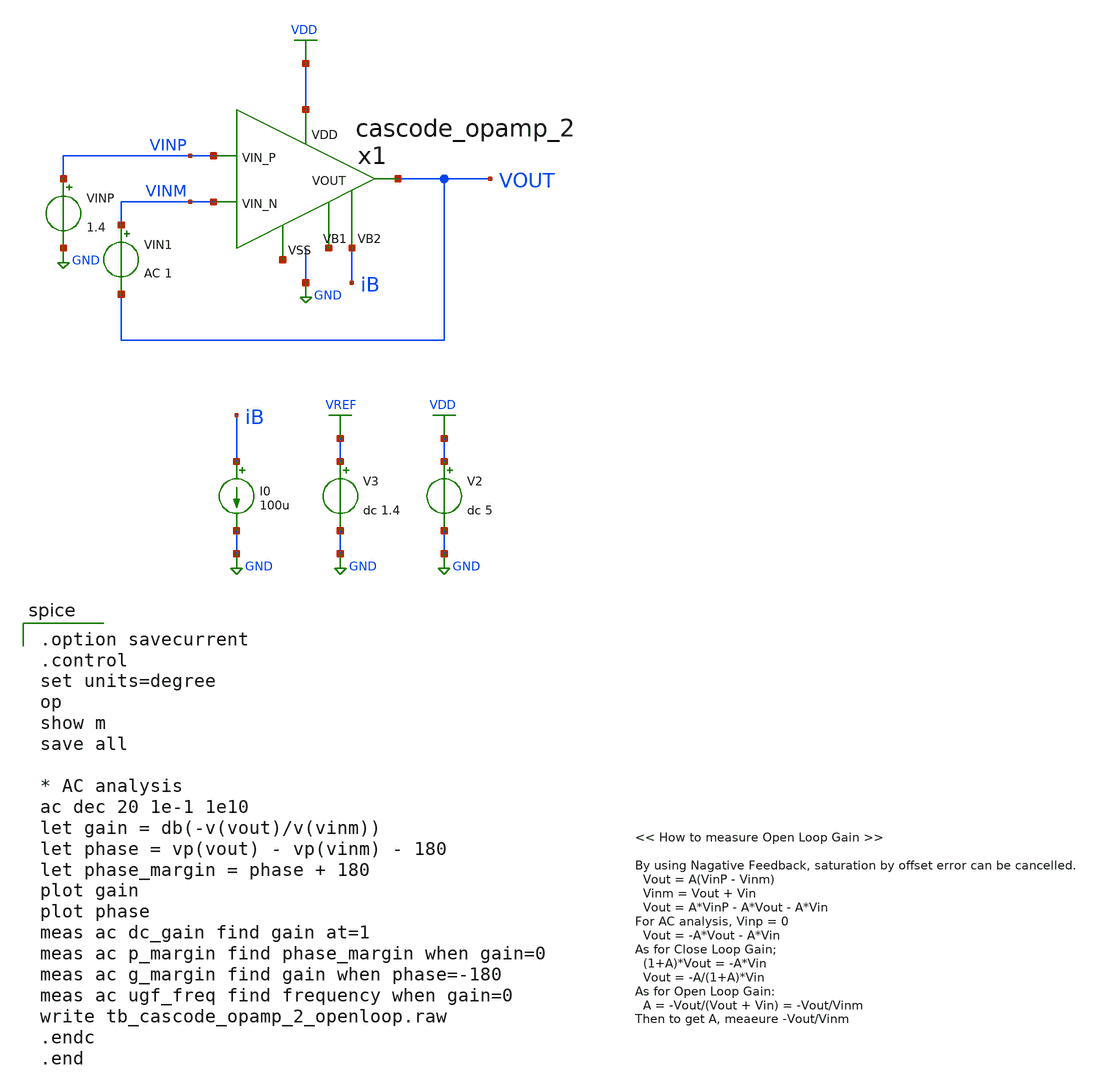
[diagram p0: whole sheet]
** sch_path: member_project/AM_Radio/Yamada3/xschem/tb_cascode_opamp_2_openloop.sch
**.subckt tb_cascode_opamp_2_openloop
V2 VDD GND dc 5
V3 VREF GND dc 1.4
I0 iB GND 100u
x1 VDD net1 VINP VINM VOUT iB net2 cascode_opamp_2
VIN1 VINM VOUT AC 1
VINP VINP GND 1.4
**** begin user architecture code
 .include $::LIB/ip62_models

.option savecurrent
.control
set units=degree
op
show m
save all

* AC analysis
ac dec 20 1e-1 1e10
let gain = db(-v(vout)/v(vinm))
let phase = vp(vout) - vp(vinm) - 180
let phase_margin = phase + 180
plot gain
plot phase
meas ac dc_gain find gain at=1
meas ac p_margin find phase_margin when gain=0
meas ac g_margin find gain when phase=-180
meas ac ugf_freq find frequency when gain=0
write tb_cascode_opamp_2_openloop.raw
.endc
.end


**** end user architecture code
**.ends

* expanding   symbol:  cascode_opamp_2.sym # of pins=7
** sym_path: member_project/AM_Radio/noritsuna/xschem/cascode_opamp_2.sym
** sch_path: member_project/AM_Radio/noritsuna/xschem/cascode_opamp_2.sch
.subckt cascode_opamp_2 VDD VSS VIN_P VIN_N VOUT VB2 VB1
*.opin VOUT
*.ipin VIN_N
*.ipin VIN_P
*.ipin VSS
*.ipin VDD
*.ipin VB1
*.ipin VB2
MM2 net2 net1 VDD VDD PMOS w=240u l=8u as=0 ad=0 ps=0 pd=0 nrd=0 nrs=0 m=1
MM4 OUT1 VB2 MN_MDMY4 VSS NMOS w=84u l=8u as=0 ad=0 ps=0 pd=0 nrd=0 nrs=0 m=1
MM7 VOUT iB VDD VDD PMOS w=2400u l=8u as=0 ad=0 ps=0 pd=0 nrd=0 nrs=0 m=1
MM8 VOUT OUT1 VSS VSS NMOS w=1680u l=8u as=0 ad=0 ps=0 pd=0 nrd=0 nrs=0 m=1
MM16 net1 net1 VDD VDD PMOS w=240u l=8u as=0 ad=0 ps=0 pd=0 nrd=0 nrs=0 m=1
MM17 OUT1 MPN_MDMY3 net2 VDD PMOS w=240u l=8u as=0 ad=0 ps=0 pd=0 nrd=0 nrs=0 m=1
MM18 MPN_MDMY3 MPN_MDMY3 net1 VDD PMOS w=240u l=8u as=0 ad=0 ps=0 pd=0 nrd=0 nrs=0 m=1
MM19 MPN_MDMY3 VB2 MN_MDMY2 VSS NMOS w=84u l=8u as=0 ad=0 ps=0 pd=0 nrd=0 nrs=0 m=1
MM20 MN_MDMY4 VIN_P MN_MDMY5 VSS NMOS w=672u l=8u as=0 ad=0 ps=0 pd=0 nrd=0 nrs=0 m=1
MM21 MN_MDMY2 VIN_N MN_MDMY5 VSS NMOS w=672u l=8u as=0 ad=0 ps=0 pd=0 nrd=0 nrs=0 m=1
MM22 MN_MDMY5 VB1 VSS VSS NMOS w=84u l=8u as=0 ad=0 ps=0 pd=0 nrd=0 nrs=0 m=1
MM3 net3 net7 OUT1 VSS NMOS w=168u l=8u as=0 ad=0 ps=0 pd=0 nrd=0 nrs=0 m=1
MM6 net4 net4 VSS VSS NMOS w=168u l=8u as=0 ad=0 ps=0 pd=0 nrd=0 nrs=0 m=1
MM13 VB2 VB2 VB1 VSS NMOS w=84u l=8u as=0 ad=0 ps=0 pd=0 nrd=0 nrs=0 m=1
MM14 VB1 VB1 VSS VSS NMOS w=84u l=8u as=0 ad=0 ps=0 pd=0 nrd=0 nrs=0 m=1
MM23 VB4 VB4 VDD VDD PMOS w=240u l=8u as=0 ad=0 ps=0 pd=0 nrd=0 nrs=0 m=1
MM24 VB2 iB net5 VDD PMOS w=240u l=8u as=0 ad=0 ps=0 pd=0 nrd=0 nrs=0 m=1
MM25 net5 VB4 VDD VDD PMOS w=240u l=8u as=0 ad=0 ps=0 pd=0 nrd=0 nrs=0 m=1
MM26 iB iB VB4 VDD PMOS w=240u l=8u as=0 ad=0 ps=0 pd=0 nrd=0 nrs=0 m=1
MM1 net7 iB net6 VDD PMOS w=240u l=8u as=0 ad=0 ps=0 pd=0 nrd=0 nrs=0 m=1
MM9 net6 VB4 VDD VDD PMOS w=240u l=8u as=0 ad=0 ps=0 pd=0 nrd=0 nrs=0 m=1
MM5 net7 net7 net4 VSS NMOS w=168u l=8u as=0 ad=0 ps=0 pd=0 nrd=0 nrs=0 m=1
XXC1 net3 VOUT VSS F_CSIO c=540f x=30u y=30u m=1
XMDMYN2 MN_MDMY2 VSS VSS VSS NMOS w=42u l=8u as=0 ad=0 ps=0 pd=0 nrd=0 nrs=0 m=2
XMDMYN3 MPN_MDMY3 VSS VSS VSS NMOS w=7u l=8u as=0 ad=0 ps=0 pd=0 nrd=0 nrs=0 m=4
XMDMYN4 MN_MDMY4 VSS VSS VSS NMOS w=42u l=8u as=0 ad=0 ps=0 pd=0 nrd=0 nrs=0 m=2
XMDMYN5 MN_MDMY5 VSS VSS VSS NMOS w=42u l=8u as=0 ad=0 ps=0 pd=0 nrd=0 nrs=0 m=2
XMDMYN6 OUT1 VSS VSS VSS NMOS w=42u l=8u as=0 ad=0 ps=0 pd=0 nrd=0 nrs=0 m=4
XMDMYP1 iB VDD VDD VDD PMOS w=20u l=8u as=0 ad=0 ps=0 pd=0 nrd=0 nrs=0 m=4
XMDMYP2 MPN_MDMY3 VDD VDD VDD PMOS w=20u l=8u as=0 ad=0 ps=0 pd=0 nrd=0 nrs=0 m=4
XMDMYP3 VDD VDD VDD VDD PMOS w=60u l=8u as=0 ad=0 ps=0 pd=0 nrd=0 nrs=0 m=4
MM10 iB VB2 net8 VSS NMOS w=84u l=8u as=0 ad=0 ps=0 pd=0 nrd=0 nrs=0 m=1
MM11 net8 VB1 VSS VSS NMOS w=84u l=8u as=0 ad=0 ps=0 pd=0 nrd=0 nrs=0 m=1
XMDMYN7 iB VSS VSS VSS NMOS w=7u l=8u as=0 ad=0 ps=0 pd=0 nrd=0 nrs=0 m=4
.ends

.GLOBAL VDD
.GLOBAL GND
.GLOBAL VREF
.end
